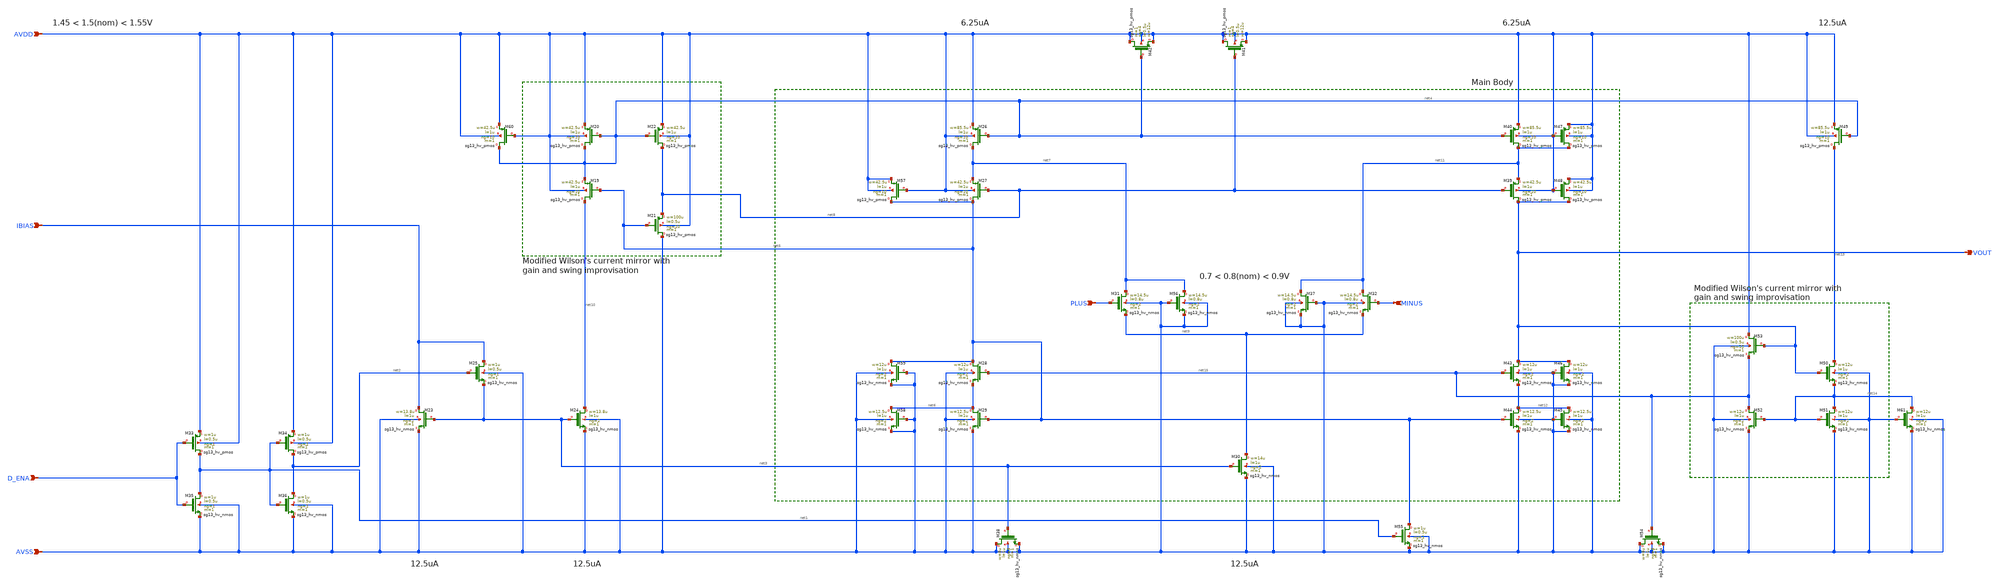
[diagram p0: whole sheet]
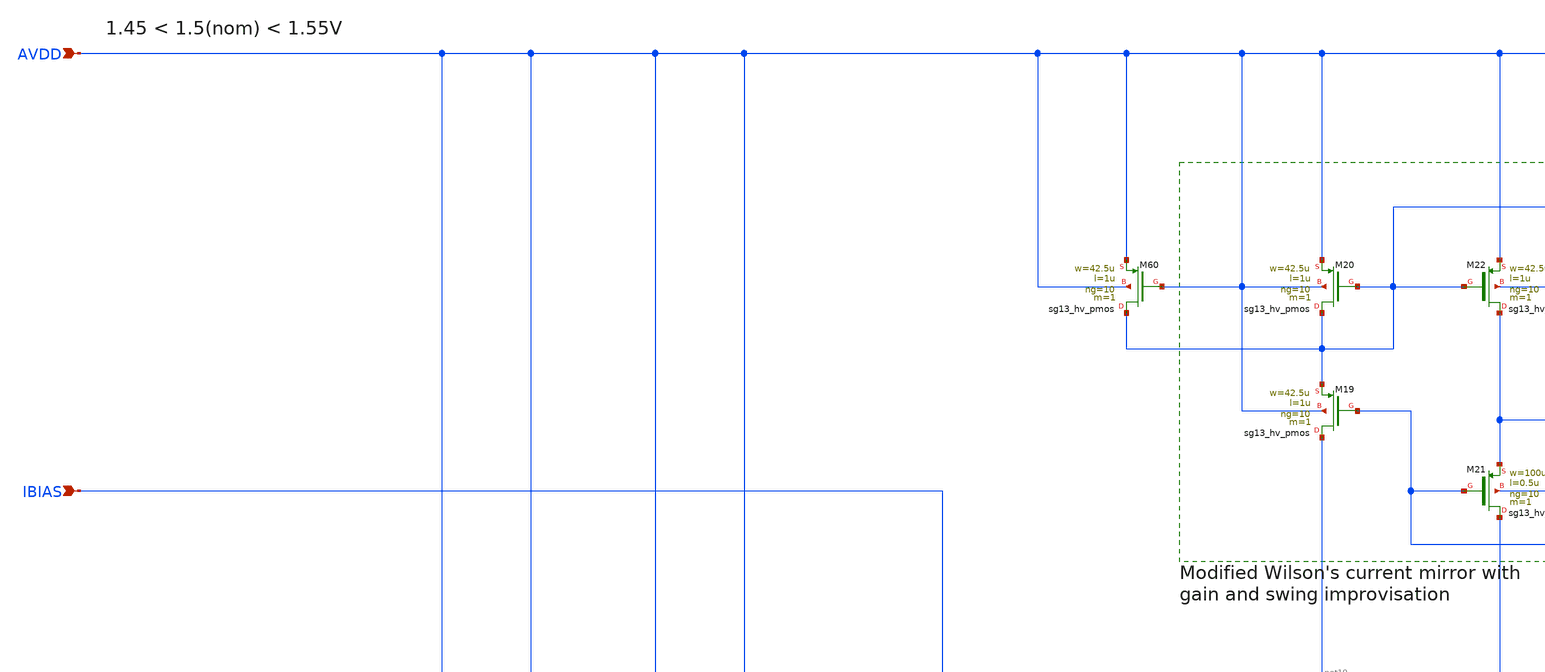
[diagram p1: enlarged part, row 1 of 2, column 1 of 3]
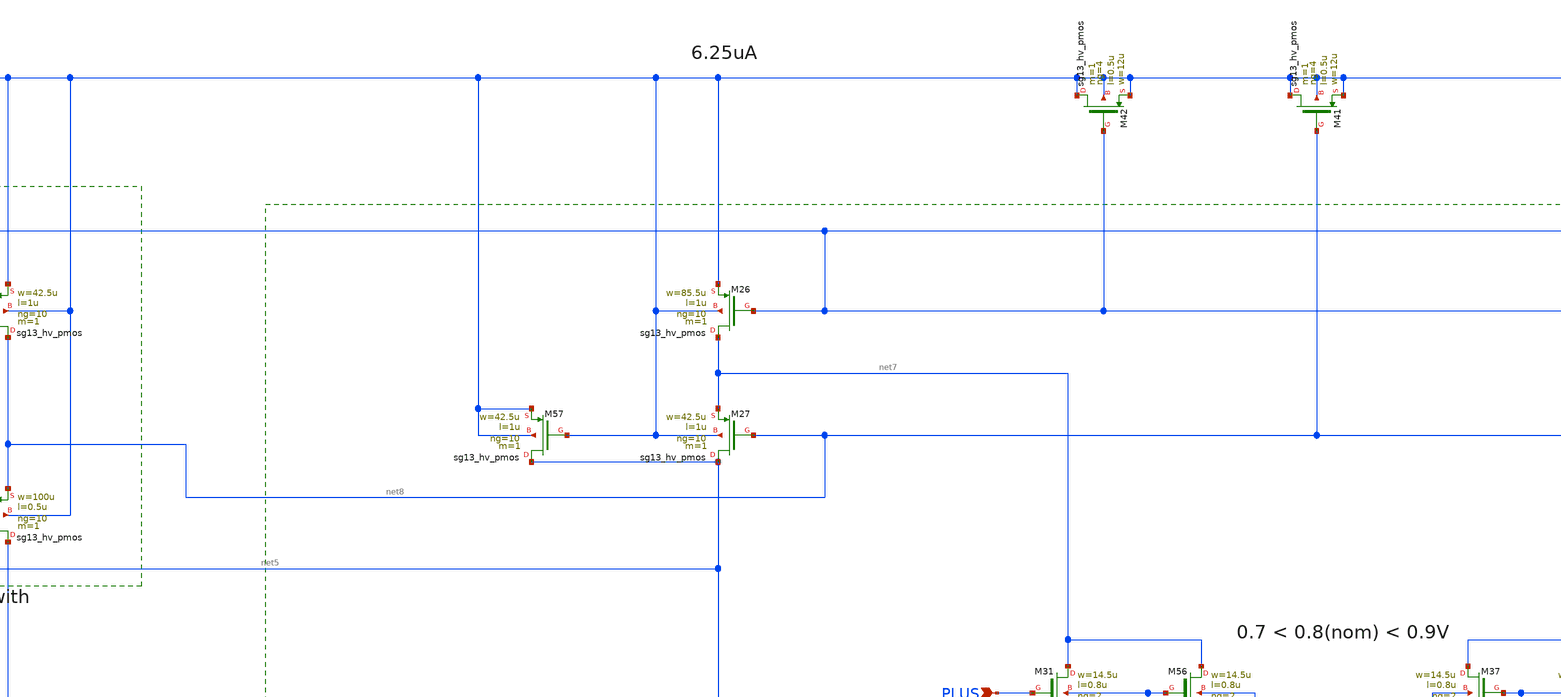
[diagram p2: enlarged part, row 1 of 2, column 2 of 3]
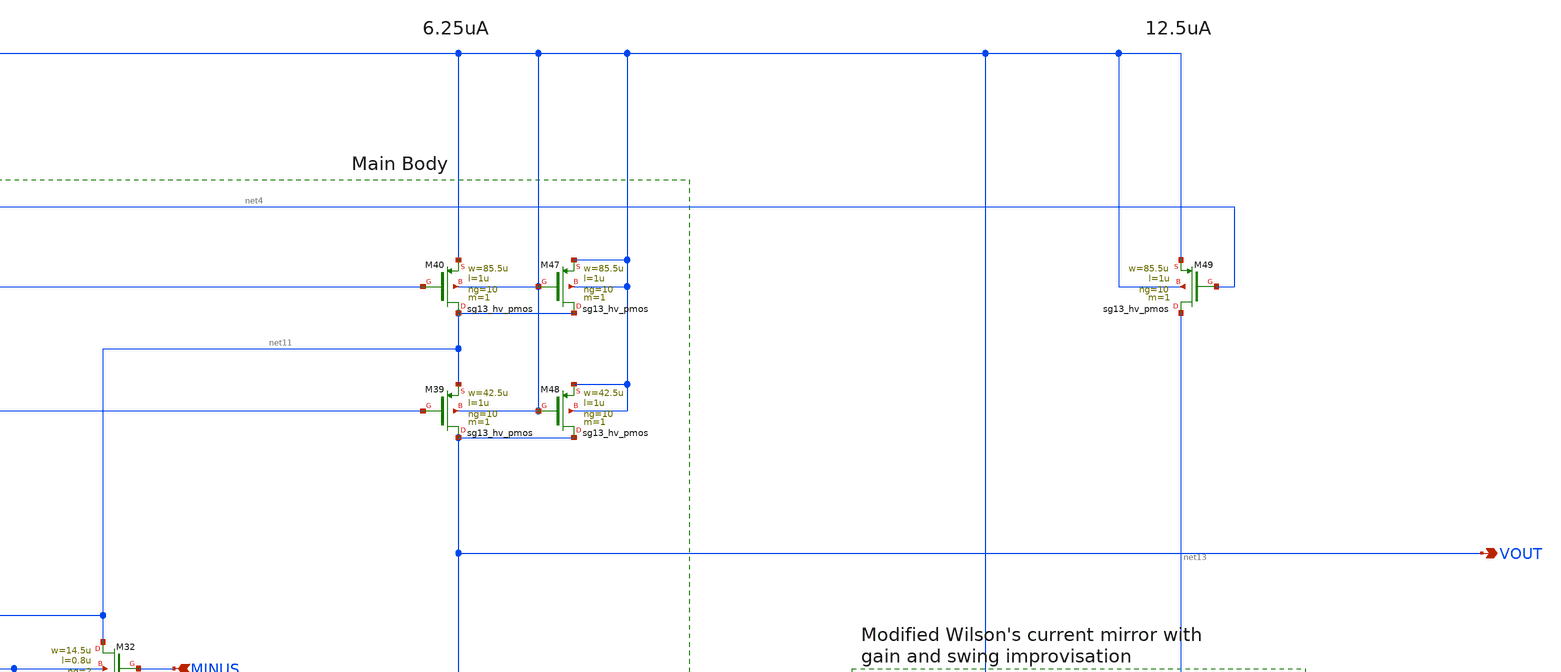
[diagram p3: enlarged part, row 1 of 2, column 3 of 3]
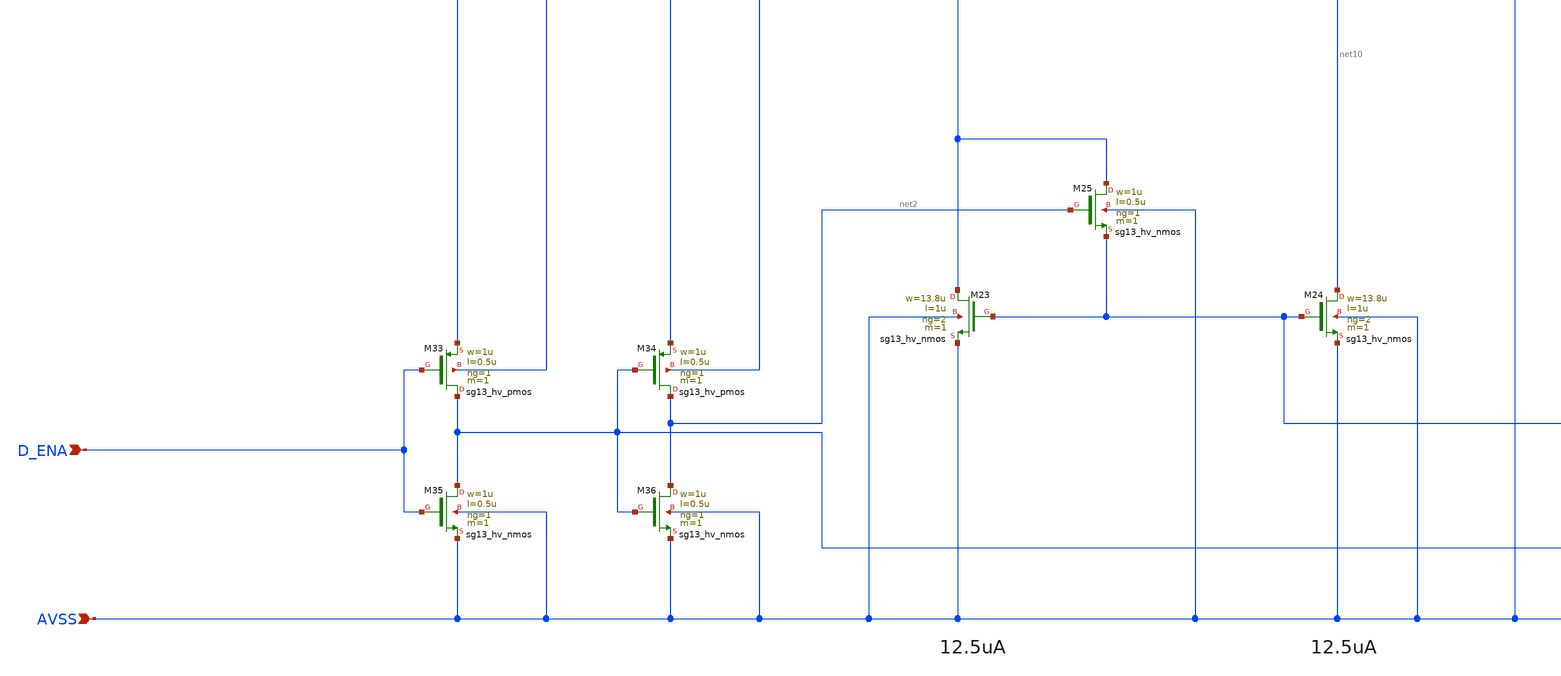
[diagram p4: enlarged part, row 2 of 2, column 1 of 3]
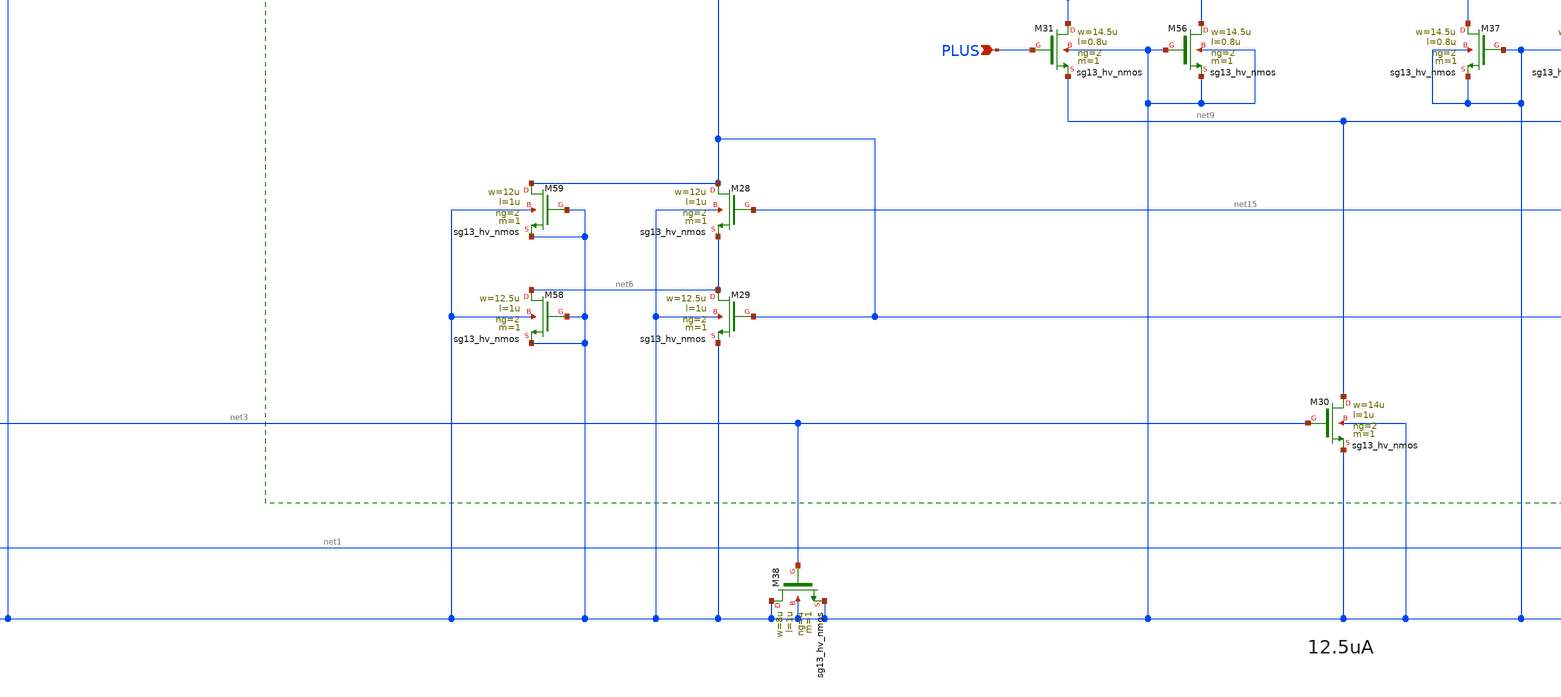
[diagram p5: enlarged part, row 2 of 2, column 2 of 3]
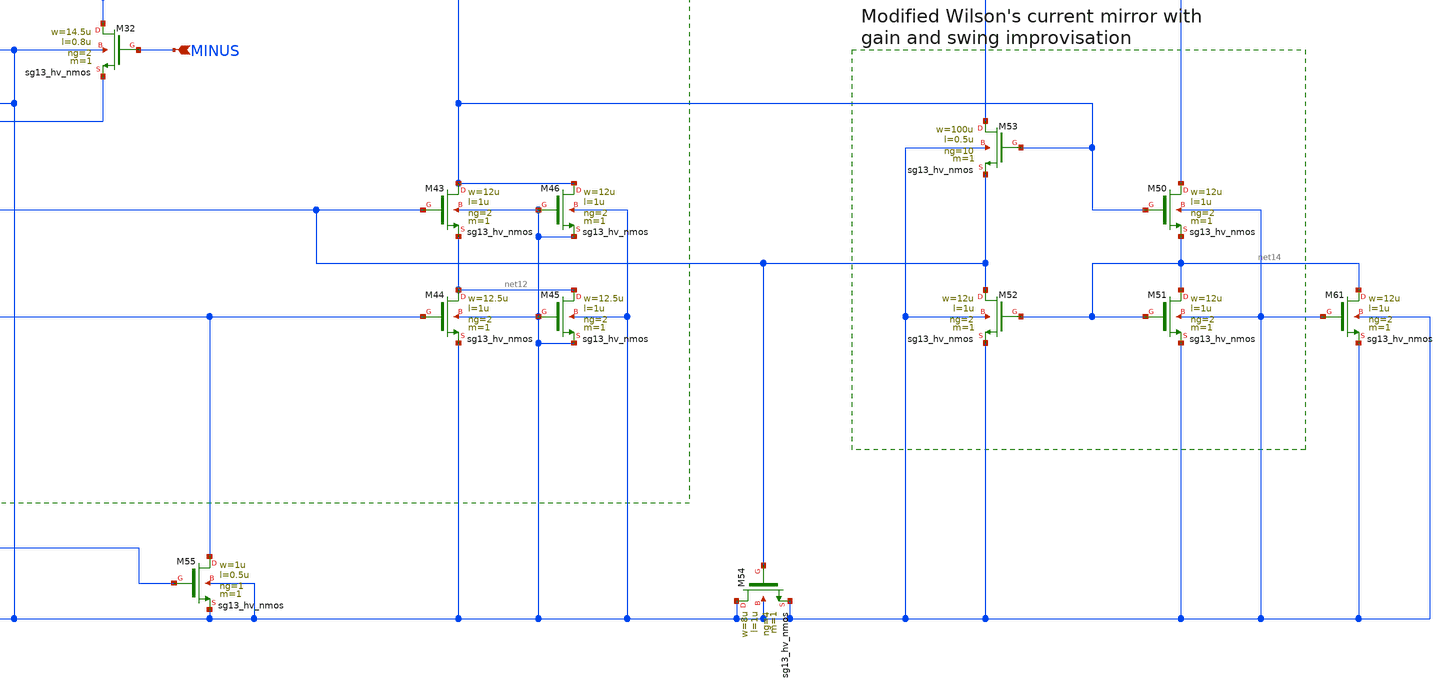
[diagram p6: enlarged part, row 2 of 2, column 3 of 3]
** sch_path: DSM_2ndOrder/1_Schematics/real_circuits/3v3/OTA1.sch
* (c) 2025 Thesis_HP, Apache-2.0 license
**.subckt OTA1 AVSS IBIAS AVDD PLUS MINUS VOUT D_ENA
*.ipin AVSS
*.ipin IBIAS
*.ipin AVDD
*.ipin PLUS
*.ipin MINUS
*.opin VOUT
*.ipin D_ENA
XM23 IBIAS net3 AVSS AVSS sg13_hv_nmos w=13.8u l=1u ng=2 m=1 mm_ok=1
XM25 IBIAS net2 net3 AVSS sg13_hv_nmos w=1u l=0.5u ng=1 m=1 mm_ok=1
XM24 net10 net3 AVSS AVSS sg13_hv_nmos w=13.8u l=1u ng=2 m=1 mm_ok=1
XM19 net10 net5 net4 AVDD sg13_hv_pmos w=42.5u l=1u ng=10 m=1 mm_ok=1
XM20 net4 net4 AVDD AVDD sg13_hv_pmos w=42.5u l=1u ng=10 m=1 mm_ok=1
XM21 AVSS net5 net8 AVDD sg13_hv_pmos w=100u l=0.5u ng=10 m=1 mm_ok=1
XM22 net8 net4 AVDD AVDD sg13_hv_pmos w=42.5u l=1u ng=10 m=1 mm_ok=1
XM26 net7 net4 AVDD AVDD sg13_hv_pmos w=85.5u l=1u ng=10 m=1 mm_ok=1
XM27 net5 net8 net7 AVDD sg13_hv_pmos w=42.5u l=1u ng=10 m=1 mm_ok=1
XM28 net5 net15 net6 AVSS sg13_hv_nmos w=12u l=1u ng=2 m=1 mm_ok=1
XM29 net6 net5 AVSS AVSS sg13_hv_nmos w=12.5u l=1u ng=2 m=1 mm_ok=1
XM30 net9 net3 AVSS AVSS sg13_hv_nmos w=14u l=1u ng=2 m=1 mm_ok=1
XM31 net7 PLUS net9 AVSS sg13_hv_nmos w=14.5u l=0.8u ng=2 m=1 mm_ok=1
XM32 net11 MINUS net9 AVSS sg13_hv_nmos w=14.5u l=0.8u ng=2 m=1 mm_ok=1
XM42 AVDD net4 AVDD AVDD sg13_hv_pmos w=12u l=0.5u ng=4 m=1 mm_ok=1
XM41 AVDD net8 AVDD AVDD sg13_hv_pmos w=12u l=0.5u ng=4 m=1 mm_ok=1
XM38 AVSS net3 AVSS AVSS sg13_hv_nmos w=8u l=1u ng=4 m=1 mm_ok=1
XM33 net1 D_ENA AVDD AVDD sg13_hv_pmos w=1u l=0.5u ng=1 m=1 mm_ok=1
XM34 net2 net1 AVDD AVDD sg13_hv_pmos w=1u l=0.5u ng=1 m=1 mm_ok=1
XM35 net1 D_ENA AVSS AVSS sg13_hv_nmos w=1u l=0.5u ng=1 m=1 mm_ok=1
XM36 net2 net1 AVSS AVSS sg13_hv_nmos w=1u l=0.5u ng=1 m=1 mm_ok=1
XM37 net11 AVSS AVSS AVSS sg13_hv_nmos w=14.5u l=0.8u ng=2 m=1 mm_ok=1
XM39 VOUT net8 net11 AVDD sg13_hv_pmos w=42.5u l=1u ng=10 m=1 mm_ok=1
XM40 net11 net4 AVDD AVDD sg13_hv_pmos w=85.5u l=1u ng=10 m=1 mm_ok=1
XM43 VOUT net15 net12 AVSS sg13_hv_nmos w=12u l=1u ng=2 m=1 mm_ok=1
XM44 net12 net5 AVSS AVSS sg13_hv_nmos w=12.5u l=1u ng=2 m=1 mm_ok=1
XM45 net12 AVSS AVSS AVSS sg13_hv_nmos w=12.5u l=1u ng=2 m=1 mm_ok=1
XM46 VOUT AVSS AVSS AVSS sg13_hv_nmos w=12u l=1u ng=2 m=1 mm_ok=1
XM47 net11 AVDD AVDD AVDD sg13_hv_pmos w=85.5u l=1u ng=10 m=1 mm_ok=1
XM48 VOUT AVDD AVDD AVDD sg13_hv_pmos w=42.5u l=1u ng=10 m=1 mm_ok=1
XM49 net13 net4 AVDD AVDD sg13_hv_pmos w=85.5u l=1u ng=10 m=1 mm_ok=1
XM50 net13 VOUT net14 AVSS sg13_hv_nmos w=12u l=1u ng=2 m=1 mm_ok=1
XM51 net14 net14 AVSS AVSS sg13_hv_nmos w=12u l=1u ng=2 m=1 mm_ok=1
XM52 net15 net14 AVSS AVSS sg13_hv_nmos w=12u l=1u ng=2 m=1 mm_ok=1
XM53 AVDD VOUT net15 AVSS sg13_hv_nmos w=100u l=0.5u ng=10 m=1 mm_ok=1
XM54 AVSS net15 AVSS AVSS sg13_hv_nmos w=8u l=1u ng=4 m=1 mm_ok=1
XM55 net5 net1 AVSS AVSS sg13_hv_nmos w=1u l=0.5u ng=1 m=1 mm_ok=1
XM56 net7 AVSS AVSS AVSS sg13_hv_nmos w=14.5u l=0.8u ng=2 m=1 mm_ok=1
XM57 net5 AVDD AVDD AVDD sg13_hv_pmos w=42.5u l=1u ng=10 m=1 mm_ok=1
XM58 net6 AVSS AVSS AVSS sg13_hv_nmos w=12.5u l=1u ng=2 m=1 mm_ok=1
XM59 net5 AVSS AVSS AVSS sg13_hv_nmos w=12u l=1u ng=2 m=1 mm_ok=1
XM60 net4 AVDD AVDD AVDD sg13_hv_pmos w=42.5u l=1u ng=10 m=1 mm_ok=1
XM61 net14 AVSS AVSS AVSS sg13_hv_nmos w=12u l=1u ng=2 m=1 mm_ok=1
**.ends
.end
